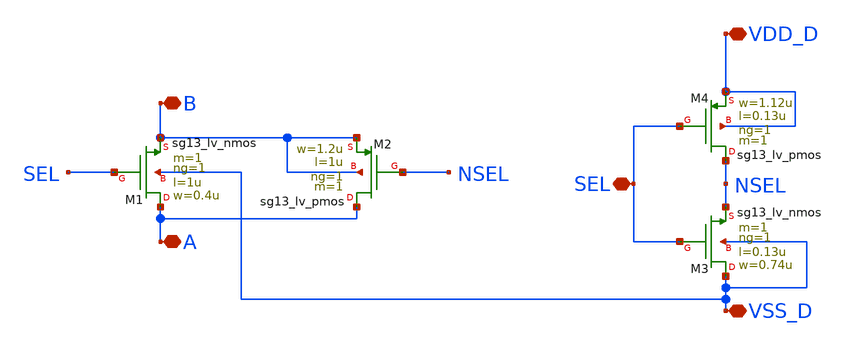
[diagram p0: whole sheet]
** sch_path: Python_layout/transmission_gate/bad_grid/tgate_inv_tx.sch
**.subckt tgate_inv_tx B SEL A VDD_D VSS_D
*.iopin B
*.iopin SEL
*.iopin A
*.iopin VDD_D
*.iopin VSS_D
XM1 A SEL B VSS_D sg13_lv_nmos w=0.4u l=1u ng=1 m=1 mm_ok=1
XM2 A NSEL B B sg13_lv_pmos w=1.2u l=1u ng=1 m=1 mm_ok=1
XM3 VSS_D SEL NSEL VSS_D sg13_lv_nmos w=0.74u l=0.13u ng=1 m=1 mm_ok=1
XM4 NSEL SEL VDD_D VDD_D sg13_lv_pmos w=1.12u l=0.13u ng=1 m=1 mm_ok=1
**.ends
.end
